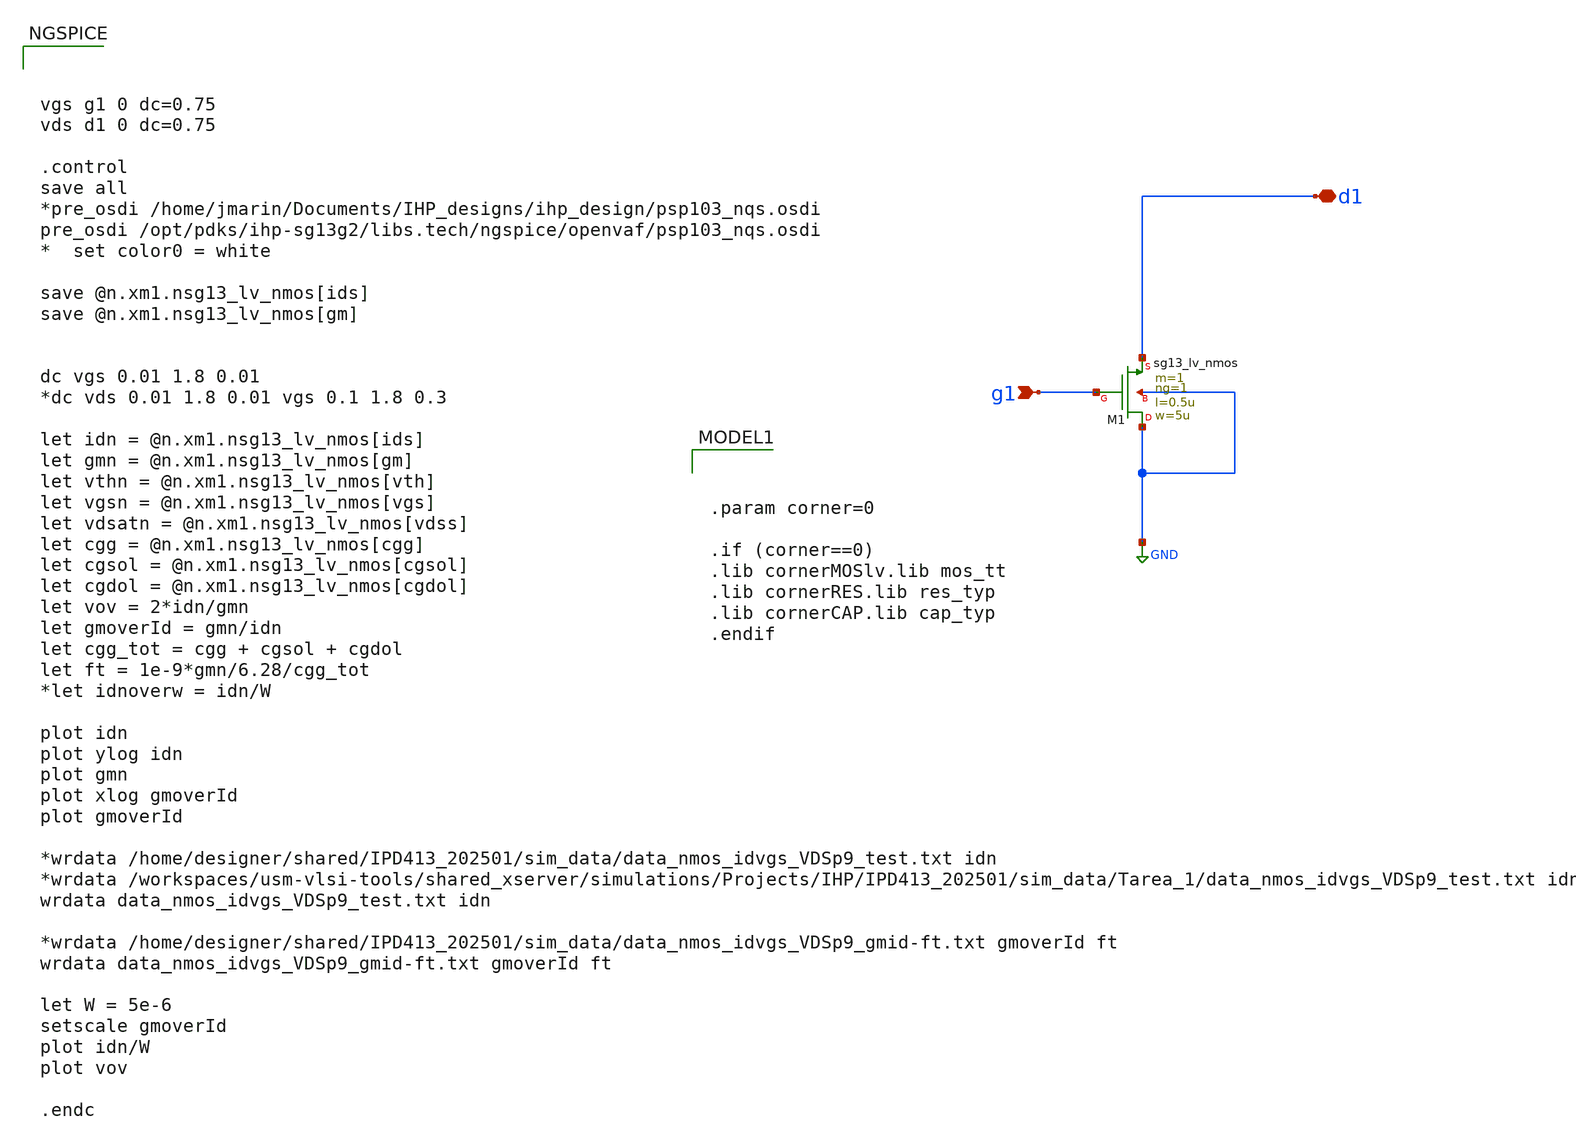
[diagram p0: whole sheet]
** sch_path: xschem/Tareas/Tarea_1/nmoslv_charac_IPD413-202501-HW1.sch
**.subckt nmoslv_charac_IPD413-202501-HW1 g1 d1
*.ipin g1
*.iopin d1
XM1 GND g1 d1 GND sg13_lv_nmos w=5u l=0.5u ng=1 m=1 mm_ok=1
**** begin user architecture code



vgs g1 0 dc=0.75
vds d1 0 dc=0.75

.control
save all
*pre_osdi /home/jmarin/Documents/IHP_designs/ihp_design/psp103_nqs.osdi
pre_osdi /opt/pdks/ihp-sg13g2/libs.tech/ngspice/openvaf/psp103_nqs.osdi
*  set color0 = white

save @n.xm1.nsg13_lv_nmos[ids]
save @n.xm1.nsg13_lv_nmos[gm]


dc vgs 0.01 1.8 0.01
*dc vds 0.01 1.8 0.01 vgs 0.1 1.8 0.3

let idn = @n.xm1.nsg13_lv_nmos[ids]
let gmn = @n.xm1.nsg13_lv_nmos[gm]
let vthn = @n.xm1.nsg13_lv_nmos[vth]
let vgsn = @n.xm1.nsg13_lv_nmos[vgs]
let vdsatn = @n.xm1.nsg13_lv_nmos[vdss]
let cgg = @n.xm1.nsg13_lv_nmos[cgg]
let cgsol = @n.xm1.nsg13_lv_nmos[cgsol]
let cgdol = @n.xm1.nsg13_lv_nmos[cgdol]
let vov = 2*idn/gmn
let gmoverId = gmn/idn
let cgg_tot = cgg + cgsol + cgdol
let ft = 1e-9*gmn/6.28/cgg_tot
*let idnoverw = idn/W

plot idn
plot ylog idn
plot gmn
plot xlog gmoverId
plot gmoverId

*wrdata /home/designer/shared/IPD413_202501/sim_data/data_nmos_idvgs_VDSp9_test.txt idn
*wrdata
*+ /workspaces/usm-vlsi-tools/shared_xserver/simulations/Projects/IHP/IPD413_202501/sim_data/Tarea_1/data_nmos_idvgs_VDSp9_test.txt idn
wrdata data_nmos_idvgs_VDSp9_test.txt idn

*wrdata /home/designer/shared/IPD413_202501/sim_data/data_nmos_idvgs_VDSp9_gmid-ft.txt gmoverId ft
wrdata data_nmos_idvgs_VDSp9_gmid-ft.txt gmoverId ft

let W = 5e-6
setscale gmoverId
plot idn/W
plot vov

.endc




.param corner=0

.if (corner==0)
.lib cornerMOSlv.lib mos_tt
.lib cornerRES.lib res_typ
.lib cornerCAP.lib cap_typ
.endif

**** end user architecture code
**.ends
.GLOBAL GND
.end
